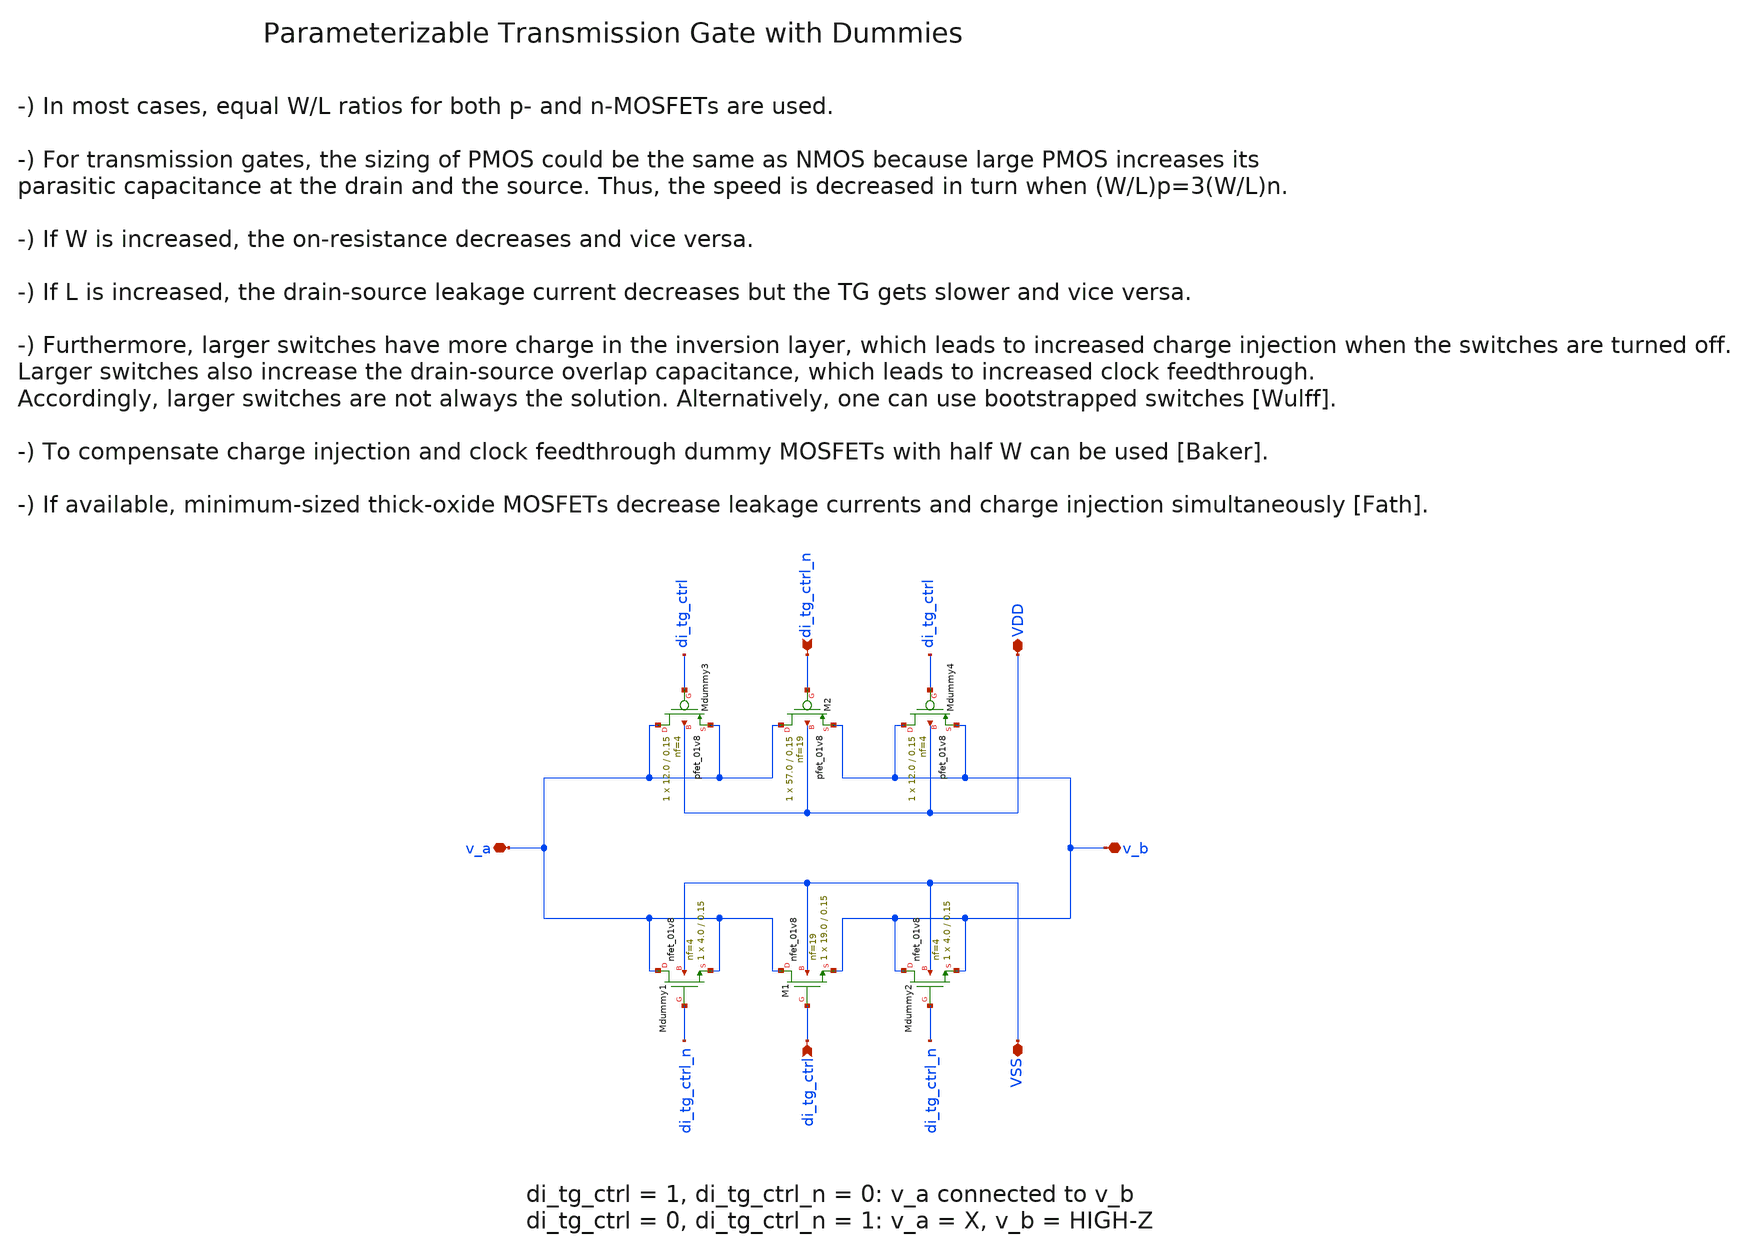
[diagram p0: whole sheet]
** sch_path: sky130/xschem/wspr_tx_iqmod_mixer_tg.sch
**.subckt wspr_tx_iqmod_mixer_tg v_a v_b VDD VSS di_tg_ctrl di_tg_ctrl_n
*.iopin v_a
*.iopin v_b
*.iopin VDD
*.iopin VSS
*.ipin di_tg_ctrl
*.ipin di_tg_ctrl_n
XM2 v_a di_tg_ctrl_n v_b VDD sky130_fd_pr__pfet_01v8 L=0.15 W=57.0 nf=19 ad='int((19 + 1)/2) * 57.0 / 19 * 0.29'
+ as='int((19 + 2)/2) * 57.0 / 19 * 0.29' pd='2*int((19 + 1)/2) * (57.0 / 19 + 0.29)' ps='2*int((19 + 2)/2) * (57.0 / 19 + 0.29)'
+ nrd='0.29 / 57.0 ' nrs='0.29 / 57.0 ' sa=0 sb=0 sd=0 mult=1 m=1
XMdummy4 v_b di_tg_ctrl v_b VDD sky130_fd_pr__pfet_01v8 L=0.15 W=12.0 nf=4 ad='int((4 + 1)/2) * 12.0 / 4 * 0.29'
+ as='int((4 + 2)/2) * 12.0 / 4 * 0.29' pd='2*int((4 + 1)/2) * (12.0 / 4 + 0.29)' ps='2*int((4 + 2)/2) * (12.0 / 4 + 0.29)'
+ nrd='0.29 / 12.0 ' nrs='0.29 / 12.0 ' sa=0 sb=0 sd=0 mult=1 m=1
XM1 v_a di_tg_ctrl v_b VSS sky130_fd_pr__nfet_01v8 L=0.15 W=19.0 nf=19 ad='int((19 + 1)/2) * 19.0 / 19 * 0.29'
+ as='int((19 + 2)/2) * 19.0 / 19 * 0.29' pd='2*int((19 + 1)/2) * (19.0 / 19 + 0.29)' ps='2*int((19 + 2)/2) * (19.0 / 19 + 0.29)'
+ nrd='0.29 / 19.0 ' nrs='0.29 / 19.0 ' sa=0 sb=0 sd=0 mult=1 m=1
XMdummy2 v_b di_tg_ctrl_n v_b VSS sky130_fd_pr__nfet_01v8 L=0.15 W=4.0 nf=4 ad='int((4 + 1)/2) * 4.0 / 4 * 0.29'
+ as='int((4 + 2)/2) * 4.0 / 4 * 0.29' pd='2*int((4 + 1)/2) * (4.0 / 4 + 0.29)' ps='2*int((4 + 2)/2) * (4.0 / 4 + 0.29)'
+ nrd='0.29 / 4.0 ' nrs='0.29 / 4.0 ' sa=0 sb=0 sd=0 mult=1 m=1
XMdummy3 v_a di_tg_ctrl v_a VDD sky130_fd_pr__pfet_01v8 L=0.15 W=12.0 nf=4 ad='int((4 + 1)/2) * 12.0 / 4 * 0.29'
+ as='int((4 + 2)/2) * 12.0 / 4 * 0.29' pd='2*int((4 + 1)/2) * (12.0 / 4 + 0.29)' ps='2*int((4 + 2)/2) * (12.0 / 4 + 0.29)'
+ nrd='0.29 / 12.0 ' nrs='0.29 / 12.0 ' sa=0 sb=0 sd=0 mult=1 m=1
XMdummy1 v_a di_tg_ctrl_n v_a VSS sky130_fd_pr__nfet_01v8 L=0.15 W=4.0 nf=4 ad='int((4 + 1)/2) * 4.0 / 4 * 0.29'
+ as='int((4 + 2)/2) * 4.0 / 4 * 0.29' pd='2*int((4 + 1)/2) * (4.0 / 4 + 0.29)' ps='2*int((4 + 2)/2) * (4.0 / 4 + 0.29)'
+ nrd='0.29 / 4.0 ' nrs='0.29 / 4.0 ' sa=0 sb=0 sd=0 mult=1 m=1
**.ends
.end
